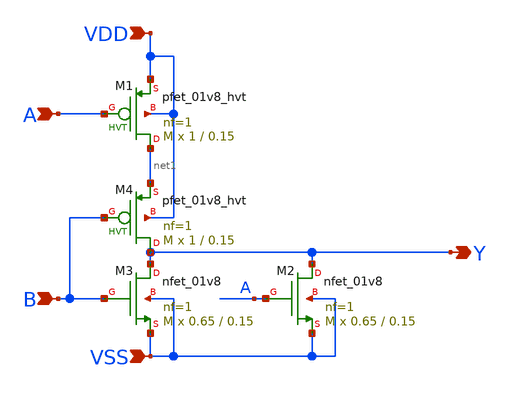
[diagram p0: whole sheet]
** sch_path: designs/nor2.sch
**.subckt nor2 A B Y VDD VSS
*.ipin A
*.ipin B
*.opin Y
*.ipin VDD
*.ipin VSS
XM2 Y A VSS VSS sky130_fd_pr__nfet_01v8 L=0.15 W=0.65 nf=1 ad='int((nf+1)/2) * W/nf * 0.29' as='int((nf+2)/2) * W/nf * 0.29'
+ pd='2*int((nf+1)/2) * (W/nf + 0.29)' ps='2*int((nf+2)/2) * (W/nf + 0.29)' nrd='0.29 / W' nrs='0.29 / W'
+ sa=0 sb=0 sd=0 mult=M m=M
XM1 net1 A VDD VDD sky130_fd_pr__pfet_01v8_hvt L=0.15 W=1 nf=1 ad='int((nf+1)/2) * W/nf * 0.29' as='int((nf+2)/2) * W/nf * 0.29'
+ pd='2*int((nf+1)/2) * (W/nf + 0.29)' ps='2*int((nf+2)/2) * (W/nf + 0.29)' nrd='0.29 / W' nrs='0.29 / W'
+ sa=0 sb=0 sd=0 mult=M m=M
XM3 Y B VSS VSS sky130_fd_pr__nfet_01v8 L=0.15 W=0.65 nf=1 ad='int((nf+1)/2) * W/nf * 0.29' as='int((nf+2)/2) * W/nf * 0.29'
+ pd='2*int((nf+1)/2) * (W/nf + 0.29)' ps='2*int((nf+2)/2) * (W/nf + 0.29)' nrd='0.29 / W' nrs='0.29 / W'
+ sa=0 sb=0 sd=0 mult=M m=M
XM4 Y B net1 VDD sky130_fd_pr__pfet_01v8_hvt L=0.15 W=1 nf=1 ad='int((nf+1)/2) * W/nf * 0.29' as='int((nf+2)/2) * W/nf * 0.29'
+ pd='2*int((nf+1)/2) * (W/nf + 0.29)' ps='2*int((nf+2)/2) * (W/nf + 0.29)' nrd='0.29 / W' nrs='0.29 / W'
+ sa=0 sb=0 sd=0 mult=M m=M
**.ends
.end
